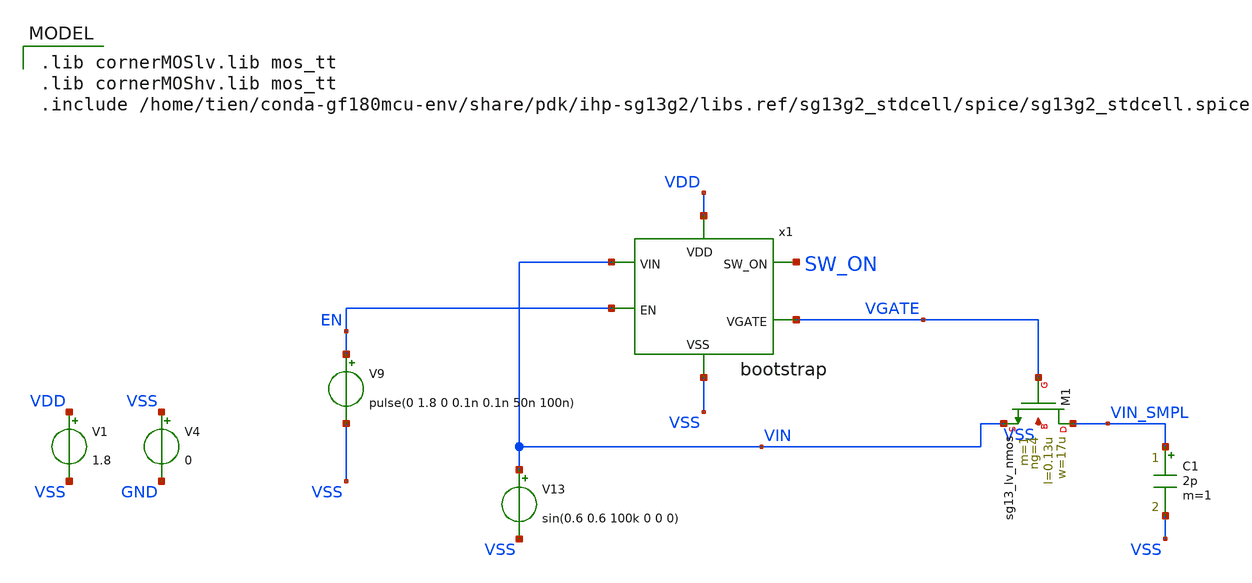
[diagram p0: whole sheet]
** sch_path: schematic/simulations/bootstrap_tb.sch
* IHP-GmbH/IHP-Open-PDK/ihp-sg13g2/libs.tech/xschem/sg13g2_stdcells/sg13g2_inv_2.sch:
* Copyright 2023 IHP PDK Authors
* Licensed under the Apache License, Version 2.0 (the "License");
**.subckt bootstrap_tb
x1 VDD VGATE VSS SW_ON VIN EN bootstrap
V9 EN VSS pulse(0 1.8 0 0.1n 0.1n 50n 100n)
V13 VIN VSS sin(0.6 0.6 100k 0 0 0)
V1 VDD VSS 1.8
.save i(v1)
V4 VSS GND 0
C1 VIN_SMPL VSS 2p m=1
XM1 VIN_SMPL VGATE VIN VSS sg13_lv_nmos w=17u l=0.13u ng=4 m=1 mm_ok=1
**** begin user architecture code
 .lib cornerMOSlv.lib mos_tt
.lib cornerMOShv.lib mos_tt
.include /home/tien/conda-gf180mcu-env/share/pdk/ihp-sg13g2/libs.ref/sg13g2_stdcell/spice/sg13g2_stdcell.spice




.option temp = 27
.save all

.option GMIN=1e-12 reltol=1e-6

.tran 10n 100u


**** end user architecture code
**.ends

* expanding   symbol:  bootstrap/bootstrap.sym # of pins=6
** sym_path: schematic/bootstrap/bootstrap.sym
** sch_path: schematic/bootstrap/bootstrap.sch
.subckt bootstrap VDD VGATE VSS SW_ON VIN EN
*.ipin VDD
*.ipin VSS
*.ipin VIN
*.ipin EN
*.opin VGATE
*.opin SW_ON
XM5 VDD VGATE Vtop Vtop sg13_lv_pmos w=0.32u l=0.15u ng=1 m=1 mm_ok=1
XM1 VGATE EN_Z_LVL_SHFT Vtop Vtop sg13_lv_pmos w=16u l=0.38u ng=4 m=1 mm_ok=1
XM2 Vtop Vbottom Vtop Vtop sg13_lv_pmos w=10u l=10u ng=2 m=1 mm_ok=1
XM6 EN_Z_LVL_SHFT EN VDD VDD sg13_lv_pmos w=0.35u l=0.15u ng=1 m=1 mm_ok=1
XM7 EN_Z_LVL_SHFT EN Vbottom VSS sg13_lv_nmos w=0.63u l=0.15u ng=1 m=1 mm_ok=1
XM8 EN_Z_LVL_SHFT VGATE Vbottom VSS sg13_lv_nmos w=1.8u l=0.15u ng=2 m=1 mm_ok=1
XM3 Vbottom EN_Z VSS VSS sg13_lv_nmos w=3.5u l=0.15u ng=1 m=1 mm_ok=1
XM10 VIN VGATE Vbottom VSS sg13_lv_nmos w=3.5u l=0.15u ng=1 m=1 mm_ok=1
XM4 net2 EN_Z VSS VSS sg13_lv_nmos w=3.5u l=0.15u ng=1 m=1 mm_ok=1
XM11 VGATE VDD VGATE_1V8 VSS sg13_lv_nmos w=3.5u l=0.45u ng=1 m=1 mm_ok=1
XM9 VGATE VDD net2 VSS sg13_hv_nmos w=6.3u l=0.45u ng=2 m=1 mm_ok=1
x2 SW_ON net1 VDD VSS sg13g2_inv_2
x4 net1 VGATE_1V8 VDD VSS sg13g2_inv_1
x1 EN_Z EN VDD VSS sg13g2_inv_1
.ends


* expanding   symbol:  sg13g2_stdcells/sg13g2_inv_2.sym # of pins=2
** sym_path: sg13g2_stdcells/sg13g2_inv_2.sym
** sch_path: sg13g2_stdcells/sg13g2_inv_2.sch
.subckt sg13g2_inv_2 Y A VDD VSS
*.opin Y
*.ipin A
*.iopin VDD
*.iopin VSS
XM1 Y A VSS VSS sg13_lv_nmos w=1.48u l=130.00n ng=2 m=1 mm_ok=1
XM2 Y A VDD VDD sg13_lv_pmos w=2.24u l=130.00n ng=2 m=1 mm_ok=1
.ends


* expanding   symbol:  sg13g2_stdcells/sg13g2_inv_1.sym # of pins=2
** sym_path: sg13g2_stdcells/sg13g2_inv_1.sym
** sch_path: sg13g2_stdcells/sg13g2_inv_1.sch
.subckt sg13g2_inv_1 Y A VDD VSS
*.opin Y
*.ipin A
*.iopin VDD
*.iopin VSS
XM1 Y A VSS VSS sg13_lv_nmos w=740.00n l=130.00n ng=1 m=1 mm_ok=1
XM2 Y A VDD VDD sg13_lv_pmos w=1.12u l=130.00n ng=1 m=1 mm_ok=1
.ends

.end
